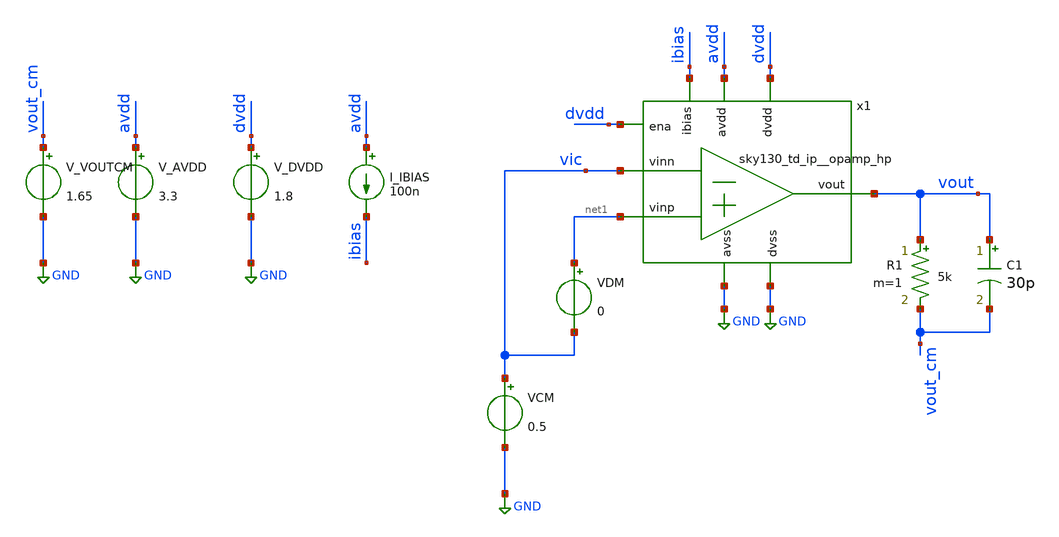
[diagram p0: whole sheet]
** sch_path: xschem/sky130_td_ip__opamp_hp_tb.sch
**.subckt sky130_td_ip__opamp_hp_tb
x1 avdd vout ibias vic net1 GND dvdd GND dvdd sky130_td_ip__opamp_hp
V_AVDD avdd GND 3.3
.save i(v_avdd)
V_DVDD dvdd GND 1.8
.save i(v_dvdd)
I_IBIAS avdd ibias 100n
VCM vic GND 0.5
R1 vout vout_cm 5k m=1
C1 vout vout_cm 30p m=1
V_VOUTCM vout_cm GND 1.65
.save i(v_voutcm)
VDM net1 vic 0
**** begin user architecture code


.dc VCM 0.1 3.2 0.1
.save all

.control
save all
run

let id1 = @m.x1.xm1.msky130_fd_pr__pfet_g5v0d10v5[id]
let id2 = @m.x1.xm2.msky130_fd_pr__pfet_g5v0d10v5[id]
let id3 = @m.x1.xm3.msky130_fd_pr__nfet_g5v0d10v5[id]
let id4 = @m.x1.xm4.msky130_fd_pr__nfet_g5v0d10v5[id]
let id11 = @m.x1.xm11.msky130_fd_pr__pfet_g5v0d10v5[id]
let id12 = @m.x1.xm12.msky130_fd_pr__pfet_g5v0d10v5[id]
let id13 = @m.x1.xm13.msky130_fd_pr__pfet_g5v0d10v5[id]
let id14 = @m.x1.xm14.msky130_fd_pr__pfet_g5v0d10v5[id]
let id15 = @m.x1.xm15.msky130_fd_pr__nfet_g5v0d10v5[id]
let id16 = @m.x1.xm16.msky130_fd_pr__nfet_g5v0d10v5[id]
let id17 = @m.x1.xm17.msky130_fd_pr__nfet_g5v0d10v5[id]
let id18 = @m.x1.xm18.msky130_fd_pr__nfet_g5v0d10v5[id]
let id19 = @m.x1.xm19.msky130_fd_pr__nfet_g5v0d10v5[id]
let id20 = @m.x1.xm20.msky130_fd_pr__pfet_g5v0d10v5[id]
let id21 = @m.x1.xm21.msky130_fd_pr__pfet_g5v0d10v5[id]
let id22 = @m.x1.xm22.msky130_fd_pr__pfet_g5v0d10v5[id]
let id23 = @m.x1.xm23.msky130_fd_pr__nfet_g5v0d10v5[id]
let id24 = @m.x1.xm24.msky130_fd_pr__nfet_g5v0d10v5[id]
let id25 = @m.x1.xm25.msky130_fd_pr__pfet_g5v0d10v5[id]
let id26 = @m.x1.xm26.msky130_fd_pr__nfet_g5v0d10v5[id]
let id27 = @m.x1.xm27.msky130_fd_pr__nfet_g5v0d10v5[id]
let id28 = @m.x1.xm28.msky130_fd_pr__pfet_g5v0d10v5[id]

let idb1 = @m.x1.xmb1.msky130_fd_pr__pfet_g5v0d10v5[id]
let idb2 = @m.x1.xmb2.msky130_fd_pr__pfet_g5v0d10v5[id]
let idb3 = @m.x1.xmb3.msky130_fd_pr__nfet_g5v0d10v5[id]
let idb4 = @m.x1.xmb4.msky130_fd_pr__nfet_g5v0d10v5[id]
let idb5 = @m.x1.xmb5.msky130_fd_pr__pfet_g5v0d10v5[id]
let idb6 = @m.x1.xmb6.msky130_fd_pr__pfet_g5v0d10v5[id]
let idb7 = @m.x1.xmb7.msky130_fd_pr__nfet_g5v0d10v5[id]
let idb8 = @m.x1.xmb8.msky130_fd_pr__nfet_g5v0d10v5[id]


let vdsat26 = @m.x1.xm26.msky130_fd_pr__nfet_g5v0d10v5[vdsat]
let vth26 = @m.x1.xm26.msky130_fd_pr__nfet_g5v0d10v5[vth]
let vgs26 = x1.net8

let vdsat25 = @m.x1.xm25.msky130_fd_pr__pfet_g5v0d10v5[vdsat]
let vth25 = @m.x1.xm25.msky130_fd_pr__pfet_g5v0d10v5[vth]
let vgs25 = avdd - x1.net7

plot (vgs25 - vth25) (vgs26 - vth26)

.endc




.lib /usr/local/share/pdk/sky130A/libs.tech/combined/sky130.lib.spice tt


**** end user architecture code
**.ends
.GLOBAL GND
.end
